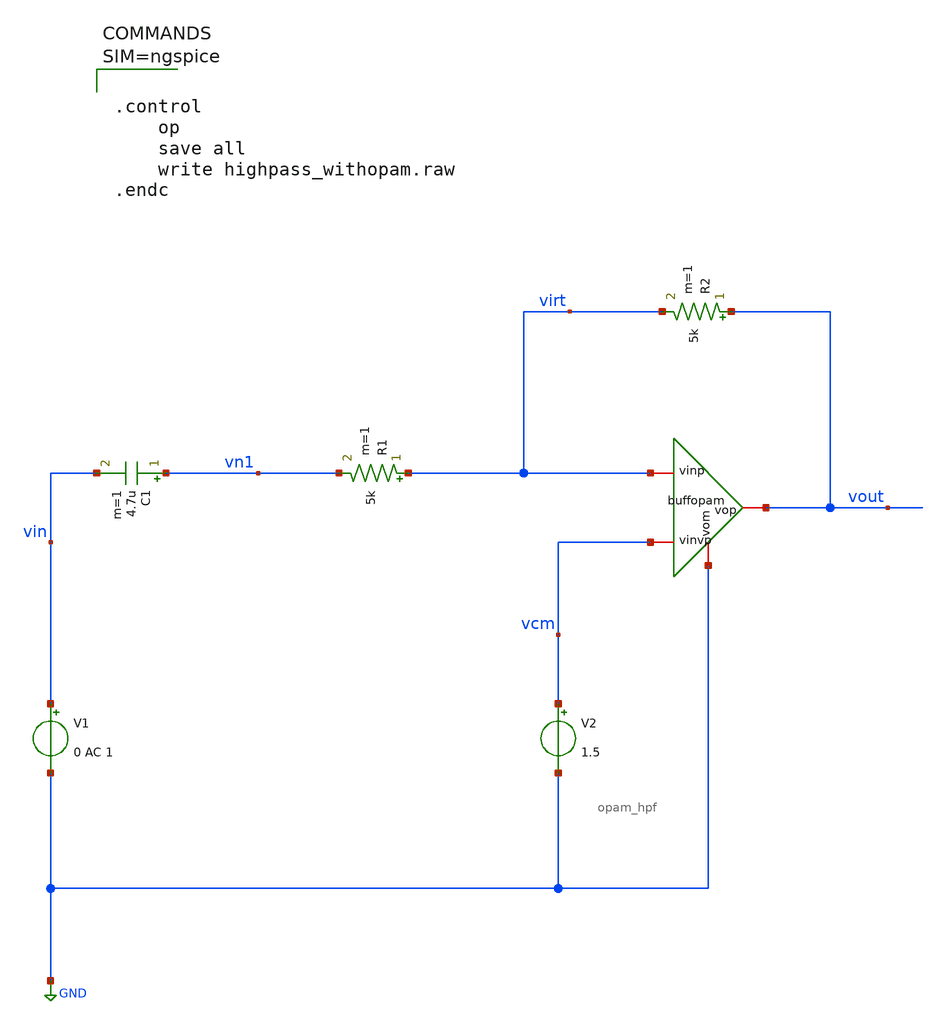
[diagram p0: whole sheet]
** sch_path: xschem/highpass_withopam.sch
**.subckt highpass_withopam
V1 vin GND 0 AC 1
C1 vn1 vin 4.7u m=1
R1 virt vn1 5k m=1
R2 vout virt 5k m=1
V2 vcm GND 1.5
x1 vout virt vcm GND opam_hpf
**** begin user architecture code



.control
	op
	save all
	write highpass_withopam.raw
.endc



**** end user architecture code
**.ends

* expanding   symbol:  /home/shubham/analoginternship/xschem-proj-1/xschem/opam_hpf.sym # of pins=4
** sym_path: xschem/opam_hpf.sym
** sch_path: xschem/opam_hpf.sch
.subckt opam_hpf vop vinp vinvp vom
*.iopin vinp
*.iopin vinvp
*.iopin vop
*.iopin vom
E1 net1 net3 vinvp vinp 1000
E2 vop vom net2 net3 1
C1 net2 net3 10n m=1
R1 net2 net1 15.9k m=1
.ends

.GLOBAL GND
.end
